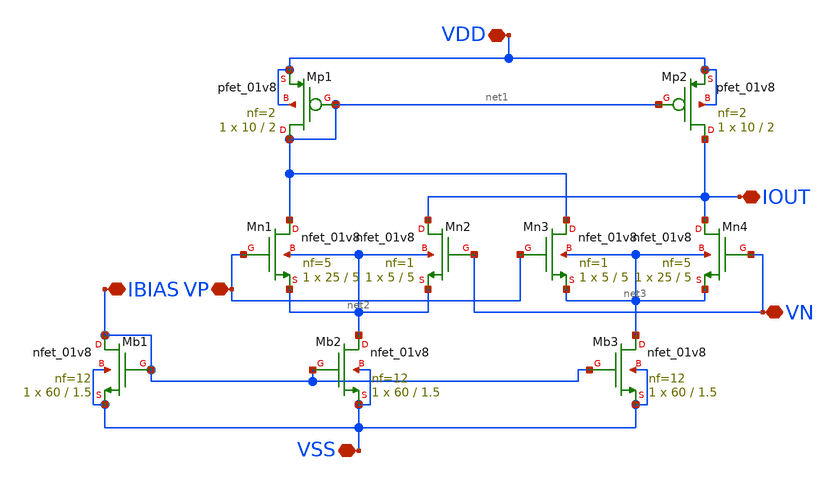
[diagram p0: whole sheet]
** sch_path: Fractional Order PID/OTA/ota3.sch
**.subckt ota3 VP IBIAS IOUT VDD VSS VN
*.iopin VP
*.iopin IBIAS
*.iopin IOUT
*.iopin VDD
*.iopin VSS
*.iopin VN
XMp1 net1 net1 VDD VDD sky130_fd_pr__pfet_01v8 L=2 W=10 nf=2 ad='int((nf+1)/2) * W/nf * 0.29' as='int((nf+2)/2) * W/nf * 0.29'
+ pd='2*int((nf+1)/2) * (W/nf + 0.29)' ps='2*int((nf+2)/2) * (W/nf + 0.29)' nrd='0.29 / W' nrs='0.29 / W'
+ sa=0 sb=0 sd=0 mult=1 m=1
XMp2 IOUT net1 VDD VDD sky130_fd_pr__pfet_01v8 L=2 W=10 nf=2 ad='int((nf+1)/2) * W/nf * 0.29' as='int((nf+2)/2) * W/nf * 0.29'
+ pd='2*int((nf+1)/2) * (W/nf + 0.29)' ps='2*int((nf+2)/2) * (W/nf + 0.29)' nrd='0.29 / W' nrs='0.29 / W'
+ sa=0 sb=0 sd=0 mult=1 m=1
XMn1 net1 VP net2 net2 sky130_fd_pr__nfet_01v8 L=5 W=25 nf=5 ad='int((nf+1)/2) * W/nf * 0.29' as='int((nf+2)/2) * W/nf * 0.29'
+ pd='2*int((nf+1)/2) * (W/nf + 0.29)' ps='2*int((nf+2)/2) * (W/nf + 0.29)' nrd='0.29 / W' nrs='0.29 / W'
+ sa=0 sb=0 sd=0 mult=1 m=1
XMn2 IOUT VN net2 net2 sky130_fd_pr__nfet_01v8 L=5 W=5 nf=1 ad='int((nf+1)/2) * W/nf * 0.29' as='int((nf+2)/2) * W/nf * 0.29'
+ pd='2*int((nf+1)/2) * (W/nf + 0.29)' ps='2*int((nf+2)/2) * (W/nf + 0.29)' nrd='0.29 / W' nrs='0.29 / W'
+ sa=0 sb=0 sd=0 mult=1 m=1
XMn3 net1 VP net3 net3 sky130_fd_pr__nfet_01v8 L=5 W=5 nf=1 ad='int((nf+1)/2) * W/nf * 0.29' as='int((nf+2)/2) * W/nf * 0.29'
+ pd='2*int((nf+1)/2) * (W/nf + 0.29)' ps='2*int((nf+2)/2) * (W/nf + 0.29)' nrd='0.29 / W' nrs='0.29 / W'
+ sa=0 sb=0 sd=0 mult=1 m=1
XMn4 IOUT VN net3 net3 sky130_fd_pr__nfet_01v8 L=5 W=25 nf=5 ad='int((nf+1)/2) * W/nf * 0.29' as='int((nf+2)/2) * W/nf * 0.29'
+ pd='2*int((nf+1)/2) * (W/nf + 0.29)' ps='2*int((nf+2)/2) * (W/nf + 0.29)' nrd='0.29 / W' nrs='0.29 / W'
+ sa=0 sb=0 sd=0 mult=1 m=1
XMb2 net2 IBIAS VSS VSS sky130_fd_pr__nfet_01v8 L=1.5 W=60 nf=12 ad='int((nf+1)/2) * W/nf * 0.29' as='int((nf+2)/2) * W/nf * 0.29'
+ pd='2*int((nf+1)/2) * (W/nf + 0.29)' ps='2*int((nf+2)/2) * (W/nf + 0.29)' nrd='0.29 / W' nrs='0.29 / W'
+ sa=0 sb=0 sd=0 mult=1 m=1
XMb1 IBIAS IBIAS VSS VSS sky130_fd_pr__nfet_01v8 L=1.5 W=60 nf=12 ad='int((nf+1)/2) * W/nf * 0.29' as='int((nf+2)/2) * W/nf * 0.29'
+ pd='2*int((nf+1)/2) * (W/nf + 0.29)' ps='2*int((nf+2)/2) * (W/nf + 0.29)' nrd='0.29 / W' nrs='0.29 / W'
+ sa=0 sb=0 sd=0 mult=1 m=1
XMb3 net3 IBIAS VSS VSS sky130_fd_pr__nfet_01v8 L=1.5 W=60 nf=12 ad='int((nf+1)/2) * W/nf * 0.29' as='int((nf+2)/2) * W/nf * 0.29'
+ pd='2*int((nf+1)/2) * (W/nf + 0.29)' ps='2*int((nf+2)/2) * (W/nf + 0.29)' nrd='0.29 / W' nrs='0.29 / W'
+ sa=0 sb=0 sd=0 mult=1 m=1
**.ends
.end
